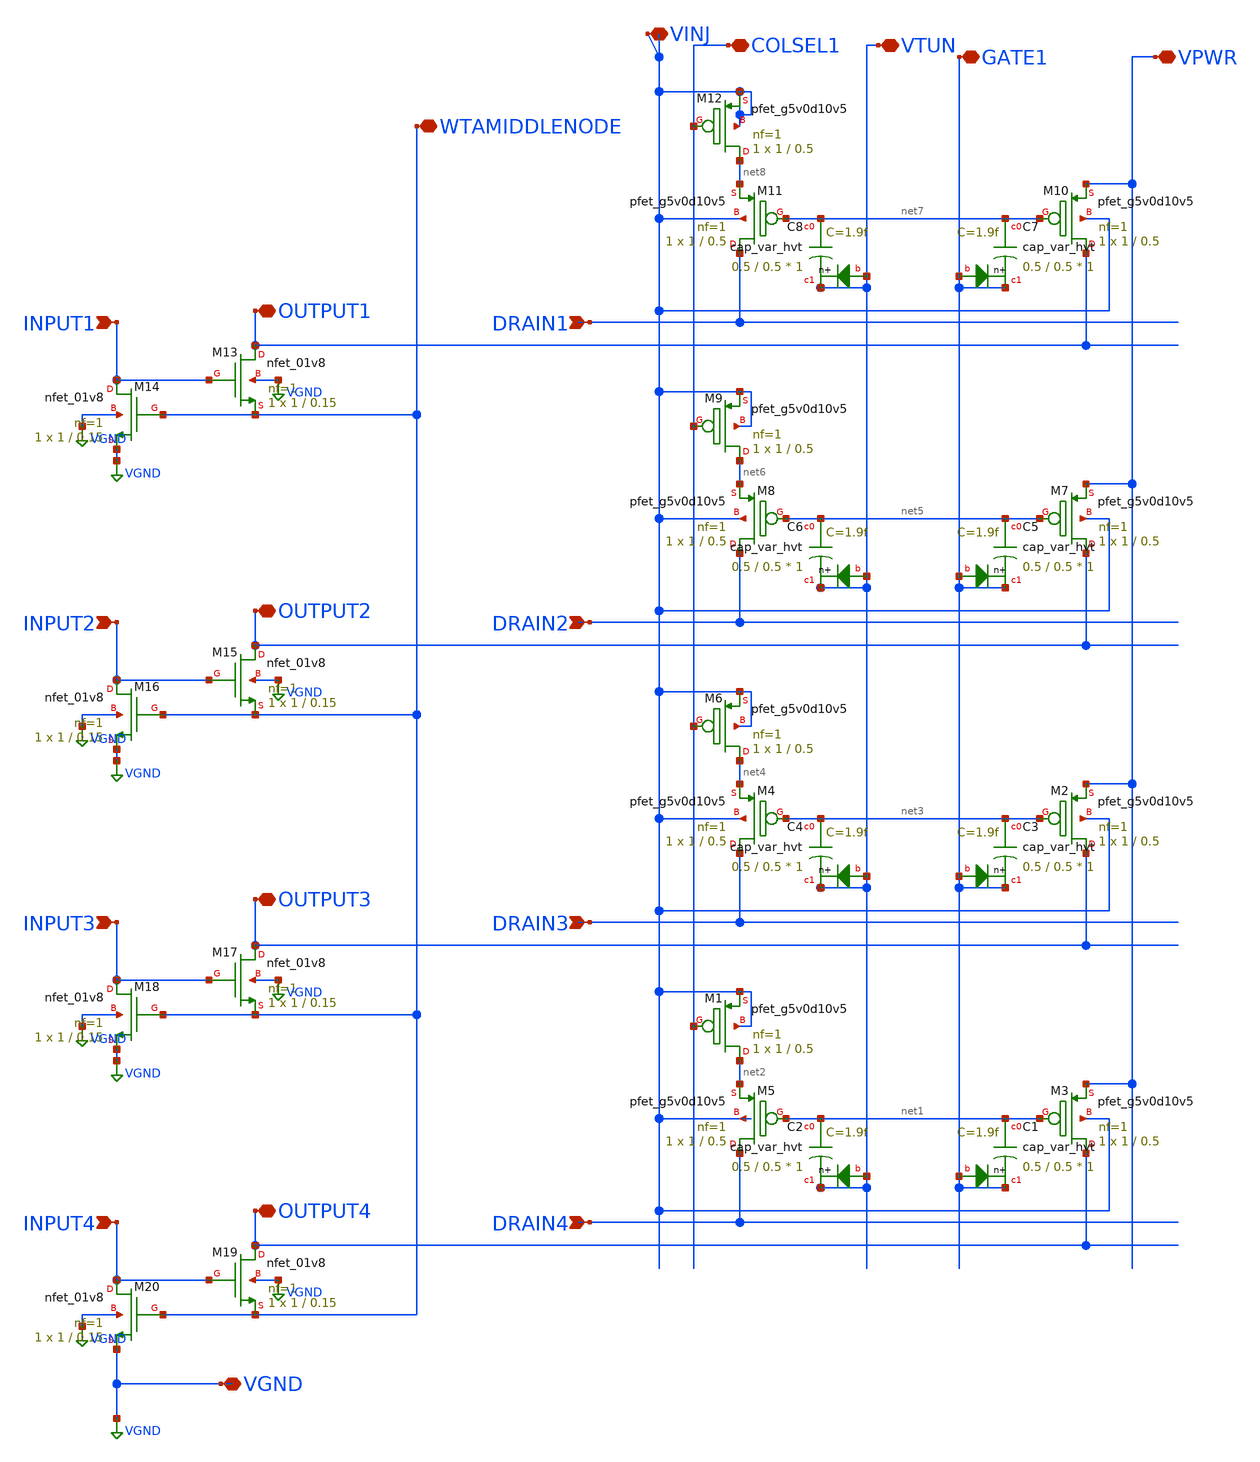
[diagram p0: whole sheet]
** sch_path: libs.ref/sky130_hilas_sc/xschem/sky130_hilas_WTA4Stage01.sch
**.subckt sky130_hilas_WTA4Stage01 DRAIN1 INPUT1 DRAIN2 DRAIN3 DRAIN4 VPWR GATE1 VTUN COLSEL1 VINJ
*+ OUTPUT1 INPUT2 OUTPUT2 INPUT3 OUTPUT3 INPUT4 OUTPUT4 WTAMIDDLENODE VGND
*.ipin DRAIN1
*.ipin INPUT1
*.ipin DRAIN2
*.ipin DRAIN3
*.ipin DRAIN4
*.iopin VPWR
*.iopin GATE1
*.iopin VTUN
*.iopin COLSEL1
*.iopin VINJ
*.iopin OUTPUT1
*.ipin INPUT2
*.iopin OUTPUT2
*.ipin INPUT3
*.iopin OUTPUT3
*.ipin INPUT4
*.iopin OUTPUT4
*.iopin WTAMIDDLENODE
*.iopin VGND
XM3 OUTPUT4 net1 VPWR VINJ sky130_fd_pr__pfet_g5v0d10v5 L=0.5 W=1 nf=1 ad='int((nf+1)/2) * W/nf * 0.29'
+ as='int((nf+2)/2) * W/nf * 0.29' pd='2*int((nf+1)/2) * (W/nf + 0.29)' ps='2*int((nf+2)/2) * (W/nf + 0.29)'
+ nrd='0.29 / W' nrs='0.29 / W' sa=0 sb=0 sd=0 mult=1 m=1
XC1 net1 GATE1 GATE1 sky130_fd_pr__cap_var_hvt W=0.5 L=0.5 VM=1 m=1
XM5 DRAIN4 net1 net2 VINJ sky130_fd_pr__pfet_g5v0d10v5 L=0.5 W=1 nf=1 ad='int((nf+1)/2) * W/nf * 0.29'
+ as='int((nf+2)/2) * W/nf * 0.29' pd='2*int((nf+1)/2) * (W/nf + 0.29)' ps='2*int((nf+2)/2) * (W/nf + 0.29)'
+ nrd='0.29 / W' nrs='0.29 / W' sa=0 sb=0 sd=0 mult=1 m=1
XC2 net1 VTUN VTUN sky130_fd_pr__cap_var_hvt W=0.5 L=0.5 VM=1 m=1
XM1 net2 COLSEL1 VINJ VINJ sky130_fd_pr__pfet_g5v0d10v5 L=0.5 W=1 nf=1 ad='int((nf+1)/2) * W/nf * 0.29'
+ as='int((nf+2)/2) * W/nf * 0.29' pd='2*int((nf+1)/2) * (W/nf + 0.29)' ps='2*int((nf+2)/2) * (W/nf + 0.29)'
+ nrd='0.29 / W' nrs='0.29 / W' sa=0 sb=0 sd=0 mult=1 m=1
XM2 OUTPUT3 net3 VPWR VINJ sky130_fd_pr__pfet_g5v0d10v5 L=0.5 W=1 nf=1 ad='int((nf+1)/2) * W/nf * 0.29'
+ as='int((nf+2)/2) * W/nf * 0.29' pd='2*int((nf+1)/2) * (W/nf + 0.29)' ps='2*int((nf+2)/2) * (W/nf + 0.29)'
+ nrd='0.29 / W' nrs='0.29 / W' sa=0 sb=0 sd=0 mult=1 m=1
XC3 net3 GATE1 GATE1 sky130_fd_pr__cap_var_hvt W=0.5 L=0.5 VM=1 m=1
XM4 DRAIN3 net3 net4 VINJ sky130_fd_pr__pfet_g5v0d10v5 L=0.5 W=1 nf=1 ad='int((nf+1)/2) * W/nf * 0.29'
+ as='int((nf+2)/2) * W/nf * 0.29' pd='2*int((nf+1)/2) * (W/nf + 0.29)' ps='2*int((nf+2)/2) * (W/nf + 0.29)'
+ nrd='0.29 / W' nrs='0.29 / W' sa=0 sb=0 sd=0 mult=1 m=1
XC4 net3 VTUN VTUN sky130_fd_pr__cap_var_hvt W=0.5 L=0.5 VM=1 m=1
XM6 net4 COLSEL1 VINJ VINJ sky130_fd_pr__pfet_g5v0d10v5 L=0.5 W=1 nf=1 ad='int((nf+1)/2) * W/nf * 0.29'
+ as='int((nf+2)/2) * W/nf * 0.29' pd='2*int((nf+1)/2) * (W/nf + 0.29)' ps='2*int((nf+2)/2) * (W/nf + 0.29)'
+ nrd='0.29 / W' nrs='0.29 / W' sa=0 sb=0 sd=0 mult=1 m=1
XM7 OUTPUT2 net5 VPWR VINJ sky130_fd_pr__pfet_g5v0d10v5 L=0.5 W=1 nf=1 ad='int((nf+1)/2) * W/nf * 0.29'
+ as='int((nf+2)/2) * W/nf * 0.29' pd='2*int((nf+1)/2) * (W/nf + 0.29)' ps='2*int((nf+2)/2) * (W/nf + 0.29)'
+ nrd='0.29 / W' nrs='0.29 / W' sa=0 sb=0 sd=0 mult=1 m=1
XC5 net5 GATE1 GATE1 sky130_fd_pr__cap_var_hvt W=0.5 L=0.5 VM=1 m=1
XM8 DRAIN2 net5 net6 VINJ sky130_fd_pr__pfet_g5v0d10v5 L=0.5 W=1 nf=1 ad='int((nf+1)/2) * W/nf * 0.29'
+ as='int((nf+2)/2) * W/nf * 0.29' pd='2*int((nf+1)/2) * (W/nf + 0.29)' ps='2*int((nf+2)/2) * (W/nf + 0.29)'
+ nrd='0.29 / W' nrs='0.29 / W' sa=0 sb=0 sd=0 mult=1 m=1
XC6 net5 VTUN VTUN sky130_fd_pr__cap_var_hvt W=0.5 L=0.5 VM=1 m=1
XM9 net6 COLSEL1 VINJ VINJ sky130_fd_pr__pfet_g5v0d10v5 L=0.5 W=1 nf=1 ad='int((nf+1)/2) * W/nf * 0.29'
+ as='int((nf+2)/2) * W/nf * 0.29' pd='2*int((nf+1)/2) * (W/nf + 0.29)' ps='2*int((nf+2)/2) * (W/nf + 0.29)'
+ nrd='0.29 / W' nrs='0.29 / W' sa=0 sb=0 sd=0 mult=1 m=1
XM10 OUTPUT1 net7 VPWR VINJ sky130_fd_pr__pfet_g5v0d10v5 L=0.5 W=1 nf=1 ad='int((nf+1)/2) * W/nf * 0.29'
+ as='int((nf+2)/2) * W/nf * 0.29' pd='2*int((nf+1)/2) * (W/nf + 0.29)' ps='2*int((nf+2)/2) * (W/nf + 0.29)'
+ nrd='0.29 / W' nrs='0.29 / W' sa=0 sb=0 sd=0 mult=1 m=1
XC7 net7 GATE1 GATE1 sky130_fd_pr__cap_var_hvt W=0.5 L=0.5 VM=1 m=1
XM11 DRAIN1 net7 net8 VINJ sky130_fd_pr__pfet_g5v0d10v5 L=0.5 W=1 nf=1 ad='int((nf+1)/2) * W/nf * 0.29'
+ as='int((nf+2)/2) * W/nf * 0.29' pd='2*int((nf+1)/2) * (W/nf + 0.29)' ps='2*int((nf+2)/2) * (W/nf + 0.29)'
+ nrd='0.29 / W' nrs='0.29 / W' sa=0 sb=0 sd=0 mult=1 m=1
XC8 net7 VTUN VTUN sky130_fd_pr__cap_var_hvt W=0.5 L=0.5 VM=1 m=1
XM12 net8 COLSEL1 VINJ VINJ sky130_fd_pr__pfet_g5v0d10v5 L=0.5 W=1 nf=1 ad='int((nf+1)/2) * W/nf * 0.29'
+ as='int((nf+2)/2) * W/nf * 0.29' pd='2*int((nf+1)/2) * (W/nf + 0.29)' ps='2*int((nf+2)/2) * (W/nf + 0.29)'
+ nrd='0.29 / W' nrs='0.29 / W' sa=0 sb=0 sd=0 mult=1 m=1
XM13 OUTPUT1 INPUT1 WTAMIDDLENODE VGND sky130_fd_pr__nfet_01v8 L=0.15 W=1 nf=1 ad='int((nf+1)/2) * W/nf * 0.29'
+ as='int((nf+2)/2) * W/nf * 0.29' pd='2*int((nf+1)/2) * (W/nf + 0.29)' ps='2*int((nf+2)/2) * (W/nf + 0.29)'
+ nrd='0.29 / W' nrs='0.29 / W' sa=0 sb=0 sd=0 mult=1 m=1
XM14 INPUT1 WTAMIDDLENODE VGND VGND sky130_fd_pr__nfet_01v8 L=0.15 W=1 nf=1 ad='int((nf+1)/2) * W/nf * 0.29'
+ as='int((nf+2)/2) * W/nf * 0.29' pd='2*int((nf+1)/2) * (W/nf + 0.29)' ps='2*int((nf+2)/2) * (W/nf + 0.29)'
+ nrd='0.29 / W' nrs='0.29 / W' sa=0 sb=0 sd=0 mult=1 m=1
XM15 OUTPUT2 INPUT2 WTAMIDDLENODE VGND sky130_fd_pr__nfet_01v8 L=0.15 W=1 nf=1 ad='int((nf+1)/2) * W/nf * 0.29'
+ as='int((nf+2)/2) * W/nf * 0.29' pd='2*int((nf+1)/2) * (W/nf + 0.29)' ps='2*int((nf+2)/2) * (W/nf + 0.29)'
+ nrd='0.29 / W' nrs='0.29 / W' sa=0 sb=0 sd=0 mult=1 m=1
XM16 INPUT2 WTAMIDDLENODE VGND VGND sky130_fd_pr__nfet_01v8 L=0.15 W=1 nf=1 ad='int((nf+1)/2) * W/nf * 0.29'
+ as='int((nf+2)/2) * W/nf * 0.29' pd='2*int((nf+1)/2) * (W/nf + 0.29)' ps='2*int((nf+2)/2) * (W/nf + 0.29)'
+ nrd='0.29 / W' nrs='0.29 / W' sa=0 sb=0 sd=0 mult=1 m=1
XM17 OUTPUT3 INPUT3 WTAMIDDLENODE VGND sky130_fd_pr__nfet_01v8 L=0.15 W=1 nf=1 ad='int((nf+1)/2) * W/nf * 0.29'
+ as='int((nf+2)/2) * W/nf * 0.29' pd='2*int((nf+1)/2) * (W/nf + 0.29)' ps='2*int((nf+2)/2) * (W/nf + 0.29)'
+ nrd='0.29 / W' nrs='0.29 / W' sa=0 sb=0 sd=0 mult=1 m=1
XM18 INPUT3 WTAMIDDLENODE VGND VGND sky130_fd_pr__nfet_01v8 L=0.15 W=1 nf=1 ad='int((nf+1)/2) * W/nf * 0.29'
+ as='int((nf+2)/2) * W/nf * 0.29' pd='2*int((nf+1)/2) * (W/nf + 0.29)' ps='2*int((nf+2)/2) * (W/nf + 0.29)'
+ nrd='0.29 / W' nrs='0.29 / W' sa=0 sb=0 sd=0 mult=1 m=1
XM19 OUTPUT4 INPUT4 WTAMIDDLENODE VGND sky130_fd_pr__nfet_01v8 L=0.15 W=1 nf=1 ad='int((nf+1)/2) * W/nf * 0.29'
+ as='int((nf+2)/2) * W/nf * 0.29' pd='2*int((nf+1)/2) * (W/nf + 0.29)' ps='2*int((nf+2)/2) * (W/nf + 0.29)'
+ nrd='0.29 / W' nrs='0.29 / W' sa=0 sb=0 sd=0 mult=1 m=1
XM20 INPUT4 WTAMIDDLENODE VGND VGND sky130_fd_pr__nfet_01v8 L=0.15 W=1 nf=1 ad='int((nf+1)/2) * W/nf * 0.29'
+ as='int((nf+2)/2) * W/nf * 0.29' pd='2*int((nf+1)/2) * (W/nf + 0.29)' ps='2*int((nf+2)/2) * (W/nf + 0.29)'
+ nrd='0.29 / W' nrs='0.29 / W' sa=0 sb=0 sd=0 mult=1 m=1
**.ends
.GLOBAL VGND
.end
